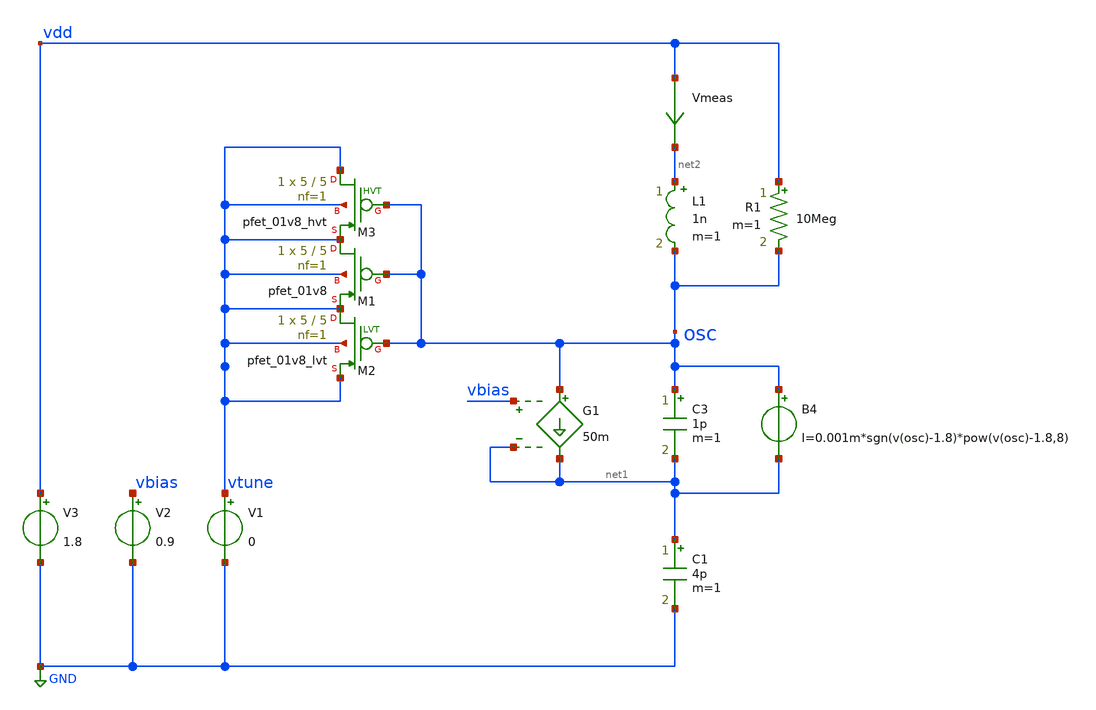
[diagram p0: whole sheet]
** sch_path: research/varactor/colpits_single.sch
**.subckt colpits_single
L1 net2 osc 1n m=1
C3 osc net1 1p m=1
G1 osc net1 vbias net1 50m
V1 vtune GND 0
V2 vbias GND 0.9
V3 vdd GND 1.8
Vmeas vdd net2 0
.save i(vmeas)
C1 net1 GND 4p m=1
B4 osc net1 I=0.001m*sgn(v(osc)-1.8)*pow(v(osc)-1.8,8)
R1 vdd osc 10Meg m=1
XM1 vtune osc vtune vtune sky130_fd_pr__pfet_01v8 L=5 W=5 nf=1 ad='int((nf+1)/2) * W/nf * 0.29' as='int((nf+2)/2) * W/nf * 0.29'
+ pd='2*int((nf+1)/2) * (W/nf + 0.29)' ps='2*int((nf+2)/2) * (W/nf + 0.29)' nrd='0.29 / W' nrs='0.29 / W'
+ sa=0 sb=0 sd=0 mult=1 m=1
XM2 vtune osc vtune vtune sky130_fd_pr__pfet_01v8_lvt L=5 W=5 nf=1 ad='int((1 + 1)/2) * 5 / 1 * 0.29'
+ as='int((1 + 2)/2) * 5 / 1 * 0.29' pd='2*int((1 + 1)/2) * (5 / 1 + 0.29)' ps='2*int((1 + 2)/2) * (5 / 1 + 0.29)'
+ nrd='0.29 / 5 ' nrs='0.29 / 5 ' sa=0 sb=0 sd=0 mult=1 m=1
XM3 vtune osc vtune vtune sky130_fd_pr__pfet_01v8_hvt L=5 W=5 nf=1 ad='int((1 + 1)/2) * 5 / 1 * 0.29'
+ as='int((1 + 2)/2) * 5 / 1 * 0.29' pd='2*int((1 + 1)/2) * (5 / 1 + 0.29)' ps='2*int((1 + 2)/2) * (5 / 1 + 0.29)'
+ nrd='0.29 / 5 ' nrs='0.29 / 5 ' sa=0 sb=0 sd=0 mult=1 m=1
**** begin user architecture code


.param temp=27
.param Vctl=0.2
.lib sky130_fd_pr/models/sky130.lib.spice tt
.inc sky130_fd_pr/cells/cap_var_hvt/sky130_fd_pr__cap_var_hvt.model.spice
.tran 1ps 40ns uic
.ic v(osc)=0.9


**** end user architecture code
**.ends
.GLOBAL GND
.end
